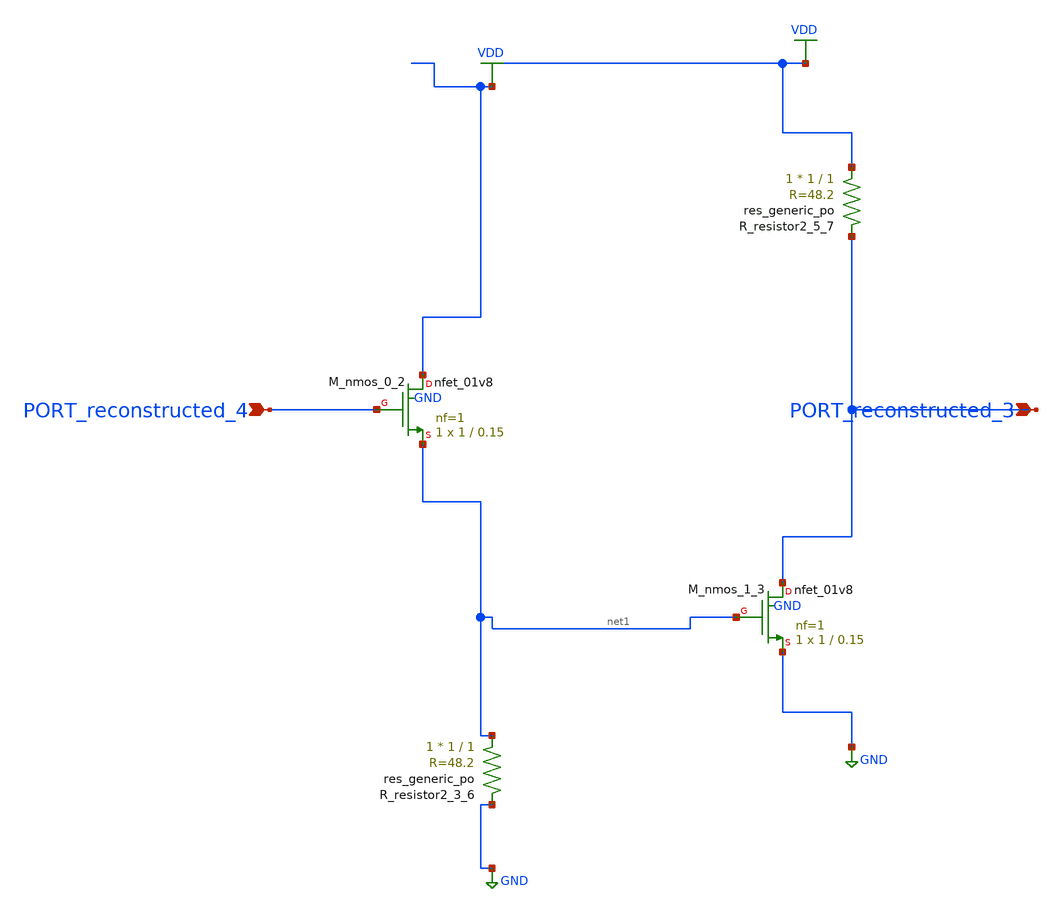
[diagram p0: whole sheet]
** sch_path: schematics/AMSNet/588.sch
**.subckt 588 PORT_reconstructed_4 PORT_reconstructed_3
*.ipin PORT_reconstructed_4
*.ipin PORT_reconstructed_3
XM_nmos_0_2 VDD PORT_reconstructed_4 net1 GND sky130_fd_pr__nfet_01v8 L=0.15 W=1 nf=1 ad='int((1 + 1)/2) * 1 / 1 * 0.29'
+ as='int((1 + 2)/2) * 1 / 1 * 0.29' pd='2*int((1 + 1)/2) * (1 / 1 + 0.29)' ps='2*int((1 + 2)/2) * (1 / 1 + 0.29)'
+ nrd='0.29 / 1 ' nrs='0.29 / 1 ' sa=0 sb=0 sd=0 mult=1 m=1
XM_nmos_1_3 PORT_reconstructed_3 net1 GND GND sky130_fd_pr__nfet_01v8 L=0.15 W=1 nf=1 ad='int((1 + 1)/2) * 1 / 1 * 0.29'
+ as='int((1 + 2)/2) * 1 / 1 * 0.29' pd='2*int((1 + 1)/2) * (1 / 1 + 0.29)' ps='2*int((1 + 2)/2) * (1 / 1 + 0.29)'
+ nrd='0.29 / 1 ' nrs='0.29 / 1 ' sa=0 sb=0 sd=0 mult=1 m=1
XR_resistor2_3_6 net1 GND sky130_fd_pr__res_generic_po W=1 L=1 m=1
XR_resistor2_5_7 VDD PORT_reconstructed_3 sky130_fd_pr__res_generic_po W=1 L=1 m=1
**.ends
.GLOBAL GND
.GLOBAL VDD
.end
